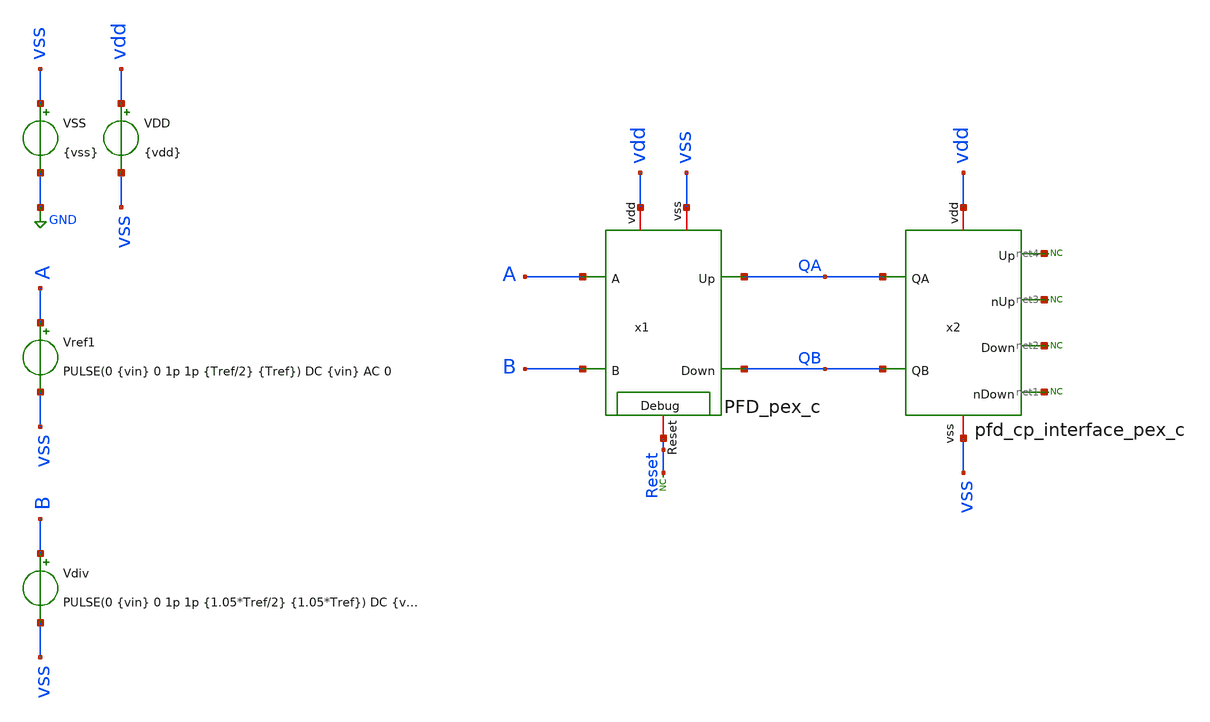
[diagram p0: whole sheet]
** sch_path: xschem/tb_PFD_pex.sch
**.subckt tb_PFD_pex
VSS vss GND {vss}
VDD vdd vss {vdd}
Vdiv B vss PULSE(0 {vin} 0 1p 1p {1.05*Tref/2} {1.05*Tref}) DC {vin} AC 0
Vref1 A vss PULSE(0 {vin} 0 1p 1p {Tref/2} {Tref}) DC {vin} AC 0
* noconn #net1
* noconn #net2
* noconn #net3
* noconn #net4
x2 net4 vdd QA net3 net2 QB vss net1 pfd_cp_interface_pex_c
x1 vss vdd QA A B QB Reset PFD_pex_c
* noconn Reset
**** begin user architecture code



* Parameters
.param kp = 0.9
.param vdd = kp*1.8
.param vss = 0.0
.param vin = vdd
.param fref = 100e6
.param Tref = 1/fref
.param C = 10f

.options TEMP = 100.0
.option RSHUNT = 1e20

* Models
.lib ~/skywater/skywater-pdk/libraries/sky130_fd_pr_ngspice/latest/models/corners/sky130.lib SS
.include ~/caravel_analog_fulgor/xschem/simulations/PFD_pex_c.spice
.include ~/caravel_analog_fulgor/xschem/simulations/pfd_cp_interface_pex_c.spice

* Data to save
.save all

.ic v(A) = 0.0
.ic v(B) = 0.0

* Simulation
.control
	tran 0.001ns 400ns
	*meas tran Tosc trig v(out) val=0.9 fall=5 targ v(out) val=0.9 fall=15
	*meas tran Td1  trig v(out) val=0.9 fall=5 targ v(out1) val=0.9 rise=6
	*meas tran Td2  trig v(out1) val=0.9 fall=5 targ v(out2) val=0.9 rise=6
	*meas tran Td3  trig v(out2) val=0.9 fall=5 targ v(out) val=0.9 rise=5
	*let  T = Tosc/10.0
	*let  f = 1/T
	*let Td = 1/(2*3*f)
	*print T f Td
	write tb_PFD_pex_tran.raw
 	plot v(Reset) v(QB)+2 v(QA)+4 v(A)+6 v(B)+6
.endc

.end


**** end user architecture code
**.ends
.GLOBAL GND
.end
